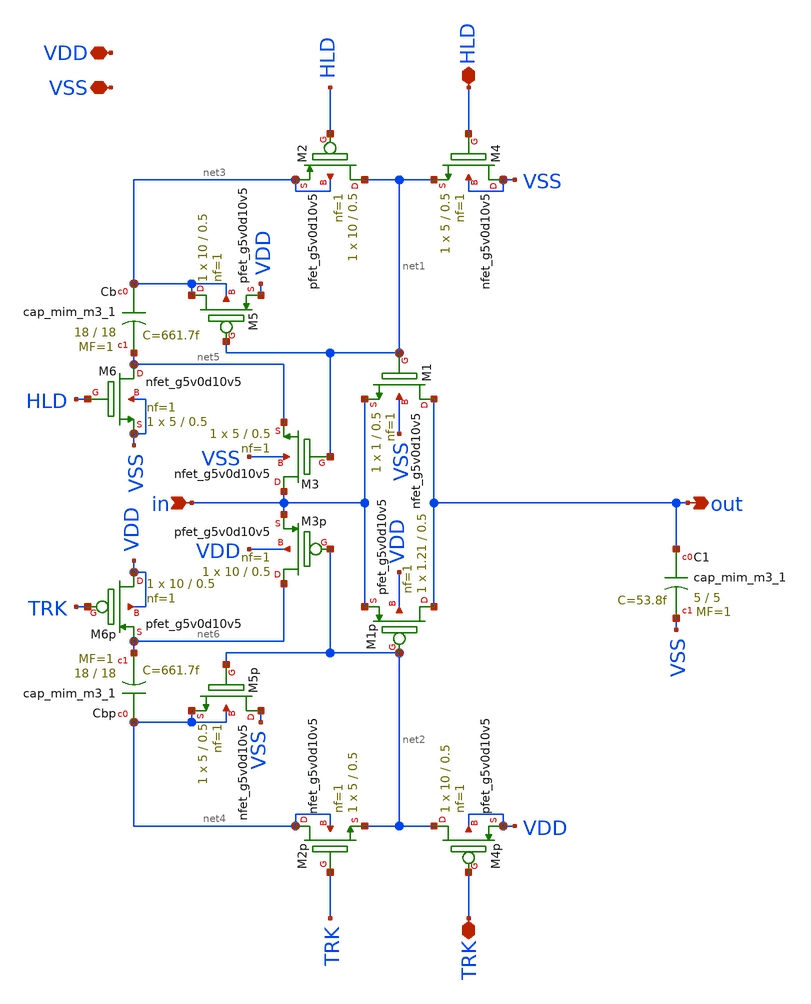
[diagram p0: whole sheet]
** sch_path: xschem/track_and_hold.sch
**.subckt track_and_hold VSS VDD in out TRK HLD
*.iopin VSS
*.iopin VDD
*.ipin in
*.opin out
*.iopin TRK
*.iopin HLD
XC1 out VSS sky130_fd_pr__cap_mim_m3_1 W=5 L=5 MF=1 m=1
XM1 out net1 in VSS sky130_fd_pr__nfet_g5v0d10v5 L=0.5 W=1 nf=1 ad='int((nf+1)/2) * W/nf * 0.29' as='int((nf+2)/2) * W/nf * 0.29'
+ pd='2*int((nf+1)/2) * (W/nf + 0.29)' ps='2*int((nf+2)/2) * (W/nf + 0.29)' nrd='0.29 / W' nrs='0.29 / W'
+ sa=0 sb=0 sd=0 mult=1 m=1
XM1p out net2 in VDD sky130_fd_pr__pfet_g5v0d10v5 L=0.5 W=1.21 nf=1 ad='int((nf+1)/2) * W/nf * 0.29'
+ as='int((nf+2)/2) * W/nf * 0.29' pd='2*int((nf+1)/2) * (W/nf + 0.29)' ps='2*int((nf+2)/2) * (W/nf + 0.29)'
+ nrd='0.29 / W' nrs='0.29 / W' sa=0 sb=0 sd=0 mult=1 m=1
XM4 VSS HLD net1 VSS sky130_fd_pr__nfet_g5v0d10v5 L=0.5 W=5 nf=1 ad='int((nf+1)/2) * W/nf * 0.29' as='int((nf+2)/2) * W/nf * 0.29'
+ pd='2*int((nf+1)/2) * (W/nf + 0.29)' ps='2*int((nf+2)/2) * (W/nf + 0.29)' nrd='0.29 / W' nrs='0.29 / W'
+ sa=0 sb=0 sd=0 mult=1 m=1
XM4p net2 TRK VDD VDD sky130_fd_pr__pfet_g5v0d10v5 L=0.5 W=10 nf=1 ad='int((nf+1)/2) * W/nf * 0.29' as='int((nf+2)/2) * W/nf * 0.29'
+ pd='2*int((nf+1)/2) * (W/nf + 0.29)' ps='2*int((nf+2)/2) * (W/nf + 0.29)' nrd='0.29 / W' nrs='0.29 / W'
+ sa=0 sb=0 sd=0 mult=1 m=1
XM2 net1 HLD net3 net3 sky130_fd_pr__pfet_g5v0d10v5 L=0.5 W=10 nf=1 ad='int((nf+1)/2) * W/nf * 0.29'
+ as='int((nf+2)/2) * W/nf * 0.29' pd='2*int((nf+1)/2) * (W/nf + 0.29)' ps='2*int((nf+2)/2) * (W/nf + 0.29)'
+ nrd='0.29 / W' nrs='0.29 / W' sa=0 sb=0 sd=0 mult=1 m=1
XM2p net4 TRK net2 net4 sky130_fd_pr__nfet_g5v0d10v5 L=0.5 W=5 nf=1 ad='int((nf+1)/2) * W/nf * 0.29'
+ as='int((nf+2)/2) * W/nf * 0.29' pd='2*int((nf+1)/2) * (W/nf + 0.29)' ps='2*int((nf+2)/2) * (W/nf + 0.29)'
+ nrd='0.29 / W' nrs='0.29 / W' sa=0 sb=0 sd=0 mult=1 m=1
XM3 in net1 net5 VSS sky130_fd_pr__nfet_g5v0d10v5 L=0.5 W=5 nf=1 ad='int((nf+1)/2) * W/nf * 0.29' as='int((nf+2)/2) * W/nf * 0.29'
+ pd='2*int((nf+1)/2) * (W/nf + 0.29)' ps='2*int((nf+2)/2) * (W/nf + 0.29)' nrd='0.29 / W' nrs='0.29 / W'
+ sa=0 sb=0 sd=0 mult=1 m=1
XM6 net5 HLD VSS VSS sky130_fd_pr__nfet_g5v0d10v5 L=0.5 W=5 nf=1 ad='int((nf+1)/2) * W/nf * 0.29' as='int((nf+2)/2) * W/nf * 0.29'
+ pd='2*int((nf+1)/2) * (W/nf + 0.29)' ps='2*int((nf+2)/2) * (W/nf + 0.29)' nrd='0.29 / W' nrs='0.29 / W'
+ sa=0 sb=0 sd=0 mult=1 m=1
XM3p net6 net2 in VDD sky130_fd_pr__pfet_g5v0d10v5 L=0.5 W=10 nf=1 ad='int((nf+1)/2) * W/nf * 0.29' as='int((nf+2)/2) * W/nf * 0.29'
+ pd='2*int((nf+1)/2) * (W/nf + 0.29)' ps='2*int((nf+2)/2) * (W/nf + 0.29)' nrd='0.29 / W' nrs='0.29 / W'
+ sa=0 sb=0 sd=0 mult=1 m=1
XM6p VDD TRK net6 VDD sky130_fd_pr__pfet_g5v0d10v5 L=0.5 W=10 nf=1 ad='int((nf+1)/2) * W/nf * 0.29' as='int((nf+2)/2) * W/nf * 0.29'
+ pd='2*int((nf+1)/2) * (W/nf + 0.29)' ps='2*int((nf+2)/2) * (W/nf + 0.29)' nrd='0.29 / W' nrs='0.29 / W'
+ sa=0 sb=0 sd=0 mult=1 m=1
XM5 net3 net1 VDD net3 sky130_fd_pr__pfet_g5v0d10v5 L=0.5 W=10 nf=1 ad='int((nf+1)/2) * W/nf * 0.29'
+ as='int((nf+2)/2) * W/nf * 0.29' pd='2*int((nf+1)/2) * (W/nf + 0.29)' ps='2*int((nf+2)/2) * (W/nf + 0.29)'
+ nrd='0.29 / W' nrs='0.29 / W' sa=0 sb=0 sd=0 mult=1 m=1
XCb net3 net5 sky130_fd_pr__cap_mim_m3_1 W=18 L=18 MF=1 m=1
XCbp net4 net6 sky130_fd_pr__cap_mim_m3_1 W=18 L=18 MF=1 m=1
XM5p VSS net2 net4 net4 sky130_fd_pr__nfet_g5v0d10v5 L=0.5 W=5 nf=1 ad='int((nf+1)/2) * W/nf * 0.29'
+ as='int((nf+2)/2) * W/nf * 0.29' pd='2*int((nf+1)/2) * (W/nf + 0.29)' ps='2*int((nf+2)/2) * (W/nf + 0.29)'
+ nrd='0.29 / W' nrs='0.29 / W' sa=0 sb=0 sd=0 mult=1 m=1
**.ends
.end
